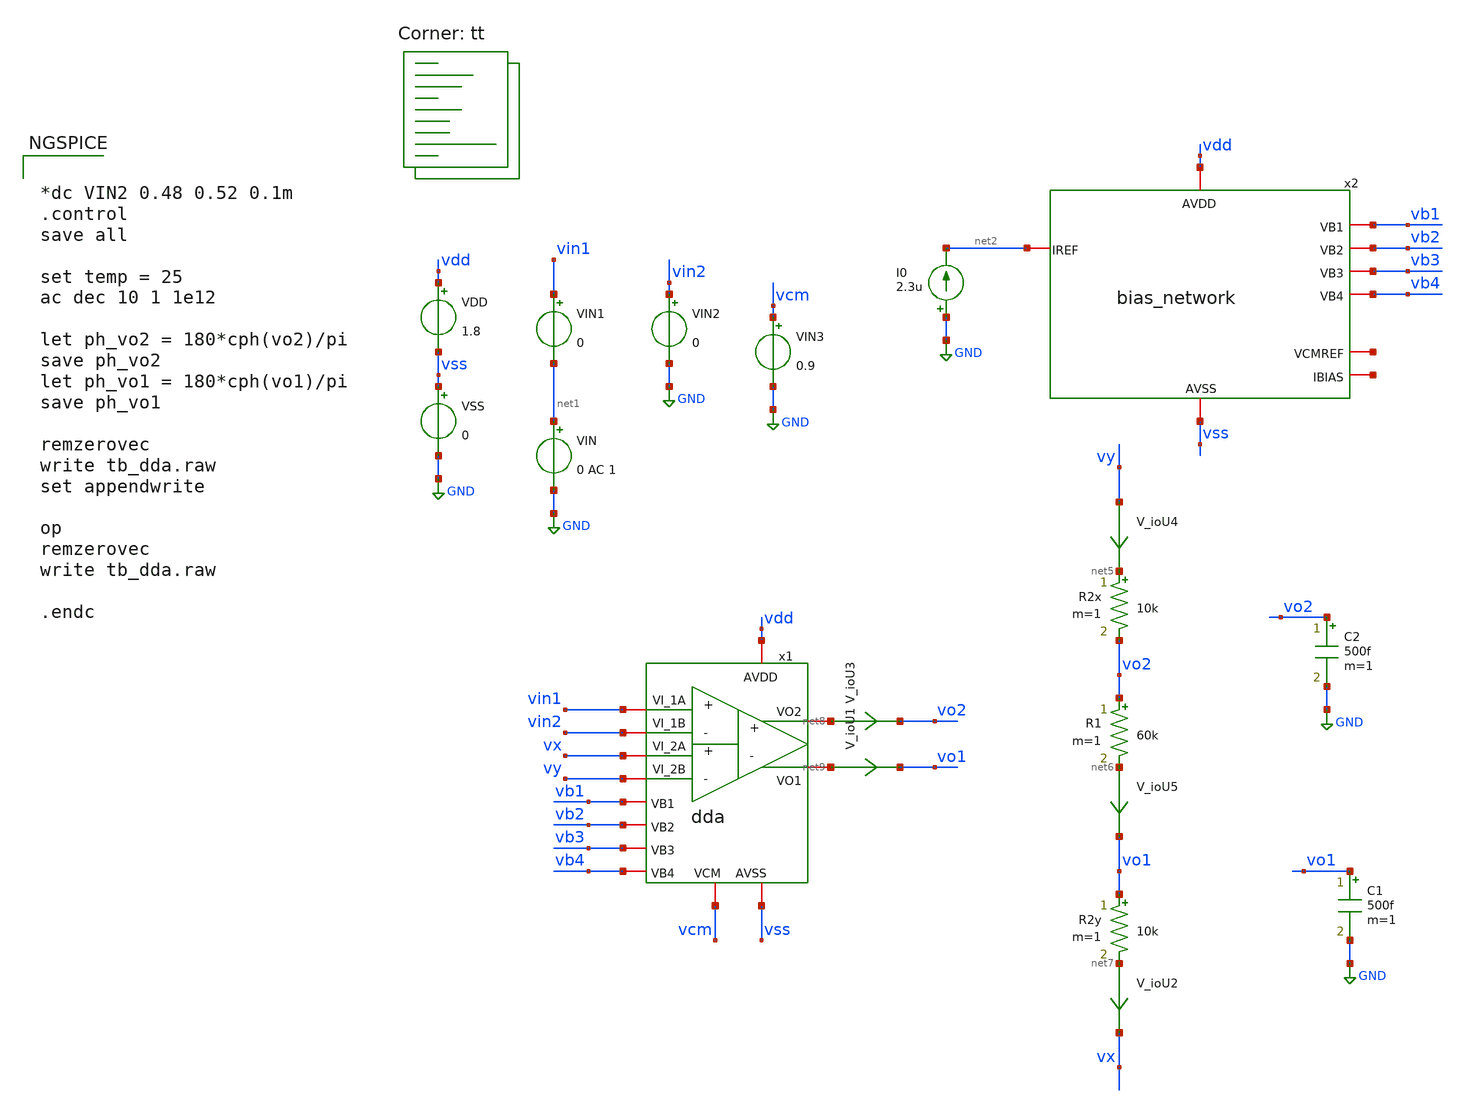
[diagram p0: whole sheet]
** sch_path: xschem/testbenches/tb_dda.sch
**.subckt tb_dda
x2 net2 vb1 vdd vss vb2 vb3 vb4 net3 net4 bias_network
VDD vdd vss 1.8
VSS vss GND 0
C1 vo1 GND 500f m=1
I0 GND net2 2.3u
VIN1 vin1 net1 0
VIN2 vin2 GND 0
VIN net1 GND 0 AC 1
C2 vo2 GND 500f m=1
VIN3 vcm GND 0.9
R2x net5 vo2 10k m=1
R1 vo2 net6 60k m=1
R2y vo1 net7 10k m=1
V_ioU3 net8 vo2 0
.save i(v_iou3)
V_ioU1 net9 vo1 0
.save i(v_iou1)
V_ioU2 net7 vx 0
.save i(v_iou2)
V_ioU4 vy net5 0
.save i(v_iou4)
V_ioU5 net6 vo1 0
.save i(v_iou5)
x1 vdd vss vin1 vin2 net8 net9 vcm vb1 vb2 vb3 vb4 vx vy dda
**** begin user architecture code


*dc VIN2 0.48 0.52 0.1m
.control
save all

set temp = 25
ac dec 10 1 1e12

let ph_vo2 = 180*cph(vo2)/pi
save ph_vo2
let ph_vo1 = 180*cph(vo1)/pi
save ph_vo1

remzerovec
write tb_dda.raw
set appendwrite

op
remzerovec
write tb_dda.raw

.endc


.lib $::SKYWATER_MODELS/sky130.lib.spice tt
**** end user architecture code
**.ends
.GLOBAL GND
.end
